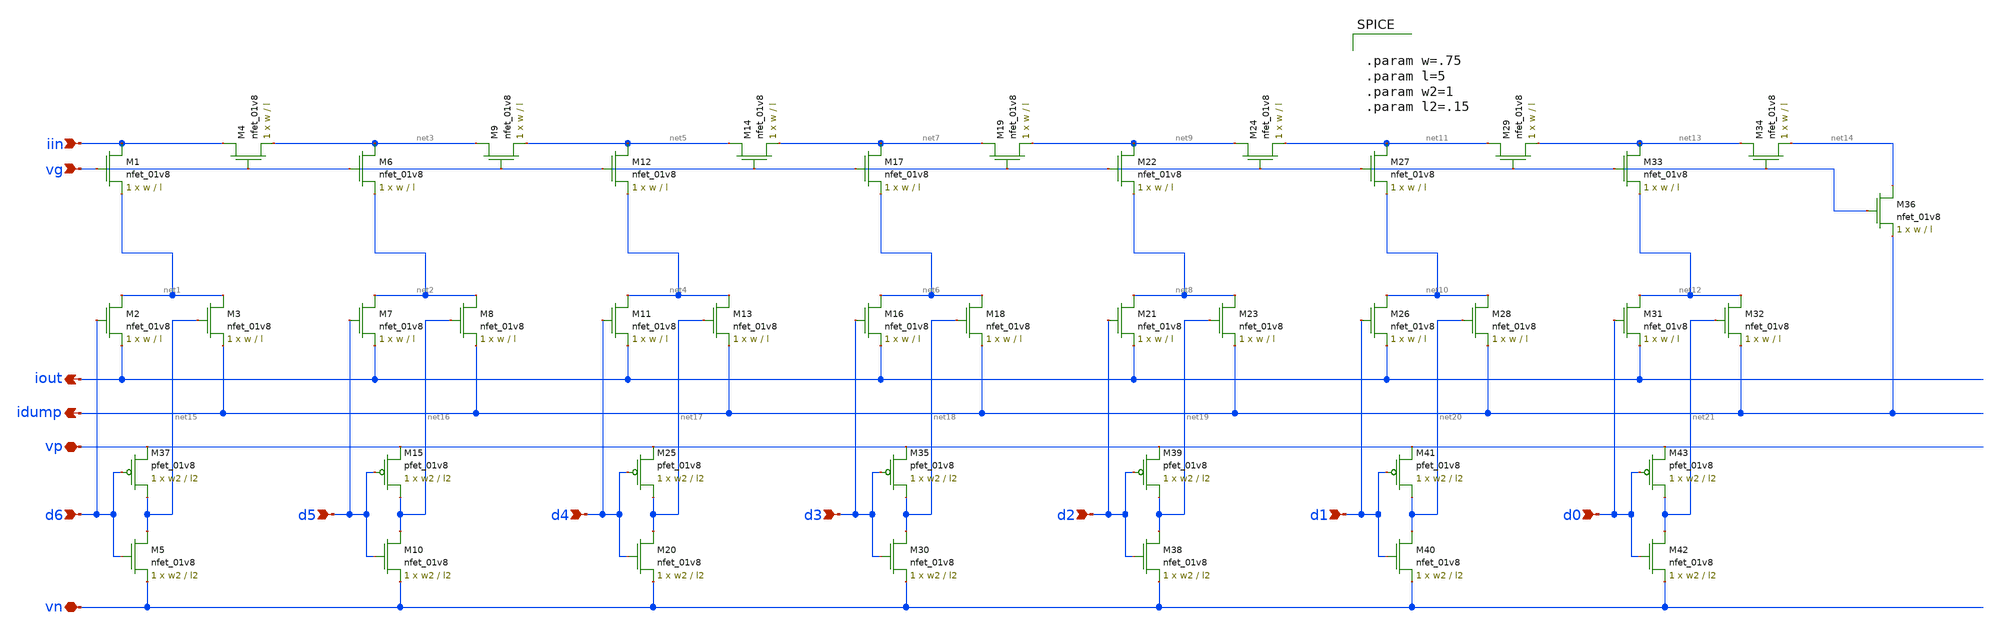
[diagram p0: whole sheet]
** sch_path: schematic/old/ladder.sch
**.subckt ladder iout idump iin vn vp d6 d5 d4 d3 d2 d1 d0 vg
*.opin iout
*.opin idump
*.ipin iin
*.iopin vn
*.iopin vp
*.ipin d6
*.ipin d5
*.ipin d4
*.ipin d3
*.ipin d2
*.ipin d1
*.ipin d0
*.ipin vg
XM1 iin vg net1 GND sky130_fd_pr__nfet_01v8 L=l W=w nf=1 ad='int((nf+1)/2) * W/nf * 0.29' as='int((nf+2)/2) * W/nf * 0.29'
+ pd='2*int((nf+1)/2) * (W/nf + 0.29)' ps='2*int((nf+2)/2) * (W/nf + 0.29)' nrd='0.29 / W' nrs='0.29 / W'
+ sa=0 sb=0 sd=0 mult=1 m=1
XM2 net1 d6 iout GND sky130_fd_pr__nfet_01v8 L=l W=w nf=1 ad='int((nf+1)/2) * W/nf * 0.29' as='int((nf+2)/2) * W/nf * 0.29'
+ pd='2*int((nf+1)/2) * (W/nf + 0.29)' ps='2*int((nf+2)/2) * (W/nf + 0.29)' nrd='0.29 / W' nrs='0.29 / W'
+ sa=0 sb=0 sd=0 mult=1 m=1
XM3 net1 net15 idump GND sky130_fd_pr__nfet_01v8 L=l W=w nf=1 ad='int((nf+1)/2) * W/nf * 0.29' as='int((nf+2)/2) * W/nf * 0.29'
+ pd='2*int((nf+1)/2) * (W/nf + 0.29)' ps='2*int((nf+2)/2) * (W/nf + 0.29)' nrd='0.29 / W' nrs='0.29 / W'
+ sa=0 sb=0 sd=0 mult=1 m=1
XM4 iin vg net3 GND sky130_fd_pr__nfet_01v8 L=l W=w nf=1 ad='int((nf+1)/2) * W/nf * 0.29' as='int((nf+2)/2) * W/nf * 0.29'
+ pd='2*int((nf+1)/2) * (W/nf + 0.29)' ps='2*int((nf+2)/2) * (W/nf + 0.29)' nrd='0.29 / W' nrs='0.29 / W'
+ sa=0 sb=0 sd=0 mult=1 m=1
XM5 net15 d6 vn GND sky130_fd_pr__nfet_01v8 L=l2 W=w2 nf=1 ad='int((nf+1)/2) * W/nf * 0.29' as='int((nf+2)/2) * W/nf * 0.29'
+ pd='2*int((nf+1)/2) * (W/nf + 0.29)' ps='2*int((nf+2)/2) * (W/nf + 0.29)' nrd='0.29 / W' nrs='0.29 / W'
+ sa=0 sb=0 sd=0 mult=1 m=1
XM6 net3 vg net2 GND sky130_fd_pr__nfet_01v8 L=l W=w nf=1 ad='int((nf+1)/2) * W/nf * 0.29' as='int((nf+2)/2) * W/nf * 0.29'
+ pd='2*int((nf+1)/2) * (W/nf + 0.29)' ps='2*int((nf+2)/2) * (W/nf + 0.29)' nrd='0.29 / W' nrs='0.29 / W'
+ sa=0 sb=0 sd=0 mult=1 m=1
XM7 net2 d5 iout GND sky130_fd_pr__nfet_01v8 L=l W=w nf=1 ad='int((nf+1)/2) * W/nf * 0.29' as='int((nf+2)/2) * W/nf * 0.29'
+ pd='2*int((nf+1)/2) * (W/nf + 0.29)' ps='2*int((nf+2)/2) * (W/nf + 0.29)' nrd='0.29 / W' nrs='0.29 / W'
+ sa=0 sb=0 sd=0 mult=1 m=1
XM8 net2 net16 idump GND sky130_fd_pr__nfet_01v8 L=l W=w nf=1 ad='int((nf+1)/2) * W/nf * 0.29' as='int((nf+2)/2) * W/nf * 0.29'
+ pd='2*int((nf+1)/2) * (W/nf + 0.29)' ps='2*int((nf+2)/2) * (W/nf + 0.29)' nrd='0.29 / W' nrs='0.29 / W'
+ sa=0 sb=0 sd=0 mult=1 m=1
XM9 net3 vg net5 GND sky130_fd_pr__nfet_01v8 L=l W=w nf=1 ad='int((nf+1)/2) * W/nf * 0.29' as='int((nf+2)/2) * W/nf * 0.29'
+ pd='2*int((nf+1)/2) * (W/nf + 0.29)' ps='2*int((nf+2)/2) * (W/nf + 0.29)' nrd='0.29 / W' nrs='0.29 / W'
+ sa=0 sb=0 sd=0 mult=1 m=1
XM11 net4 d4 iout GND sky130_fd_pr__nfet_01v8 L=l W=w nf=1 ad='int((nf+1)/2) * W/nf * 0.29' as='int((nf+2)/2) * W/nf * 0.29'
+ pd='2*int((nf+1)/2) * (W/nf + 0.29)' ps='2*int((nf+2)/2) * (W/nf + 0.29)' nrd='0.29 / W' nrs='0.29 / W'
+ sa=0 sb=0 sd=0 mult=1 m=1
XM12 net5 vg net4 GND sky130_fd_pr__nfet_01v8 L=l W=w nf=1 ad='int((nf+1)/2) * W/nf * 0.29' as='int((nf+2)/2) * W/nf * 0.29'
+ pd='2*int((nf+1)/2) * (W/nf + 0.29)' ps='2*int((nf+2)/2) * (W/nf + 0.29)' nrd='0.29 / W' nrs='0.29 / W'
+ sa=0 sb=0 sd=0 mult=1 m=1
XM13 net4 net17 idump GND sky130_fd_pr__nfet_01v8 L=l W=w nf=1 ad='int((nf+1)/2) * W/nf * 0.29' as='int((nf+2)/2) * W/nf * 0.29'
+ pd='2*int((nf+1)/2) * (W/nf + 0.29)' ps='2*int((nf+2)/2) * (W/nf + 0.29)' nrd='0.29 / W' nrs='0.29 / W'
+ sa=0 sb=0 sd=0 mult=1 m=1
XM14 net5 vg net7 GND sky130_fd_pr__nfet_01v8 L=l W=w nf=1 ad='int((nf+1)/2) * W/nf * 0.29' as='int((nf+2)/2) * W/nf * 0.29'
+ pd='2*int((nf+1)/2) * (W/nf + 0.29)' ps='2*int((nf+2)/2) * (W/nf + 0.29)' nrd='0.29 / W' nrs='0.29 / W'
+ sa=0 sb=0 sd=0 mult=1 m=1
XM16 net6 d3 iout GND sky130_fd_pr__nfet_01v8 L=l W=w nf=1 ad='int((nf+1)/2) * W/nf * 0.29' as='int((nf+2)/2) * W/nf * 0.29'
+ pd='2*int((nf+1)/2) * (W/nf + 0.29)' ps='2*int((nf+2)/2) * (W/nf + 0.29)' nrd='0.29 / W' nrs='0.29 / W'
+ sa=0 sb=0 sd=0 mult=1 m=1
XM17 net7 vg net6 GND sky130_fd_pr__nfet_01v8 L=l W=w nf=1 ad='int((nf+1)/2) * W/nf * 0.29' as='int((nf+2)/2) * W/nf * 0.29'
+ pd='2*int((nf+1)/2) * (W/nf + 0.29)' ps='2*int((nf+2)/2) * (W/nf + 0.29)' nrd='0.29 / W' nrs='0.29 / W'
+ sa=0 sb=0 sd=0 mult=1 m=1
XM18 net6 net18 idump GND sky130_fd_pr__nfet_01v8 L=l W=w nf=1 ad='int((nf+1)/2) * W/nf * 0.29' as='int((nf+2)/2) * W/nf * 0.29'
+ pd='2*int((nf+1)/2) * (W/nf + 0.29)' ps='2*int((nf+2)/2) * (W/nf + 0.29)' nrd='0.29 / W' nrs='0.29 / W'
+ sa=0 sb=0 sd=0 mult=1 m=1
XM19 net7 vg net9 GND sky130_fd_pr__nfet_01v8 L=l W=w nf=1 ad='int((nf+1)/2) * W/nf * 0.29' as='int((nf+2)/2) * W/nf * 0.29'
+ pd='2*int((nf+1)/2) * (W/nf + 0.29)' ps='2*int((nf+2)/2) * (W/nf + 0.29)' nrd='0.29 / W' nrs='0.29 / W'
+ sa=0 sb=0 sd=0 mult=1 m=1
XM21 net8 d2 iout GND sky130_fd_pr__nfet_01v8 L=l W=w nf=1 ad='int((nf+1)/2) * W/nf * 0.29' as='int((nf+2)/2) * W/nf * 0.29'
+ pd='2*int((nf+1)/2) * (W/nf + 0.29)' ps='2*int((nf+2)/2) * (W/nf + 0.29)' nrd='0.29 / W' nrs='0.29 / W'
+ sa=0 sb=0 sd=0 mult=1 m=1
XM22 net9 vg net8 GND sky130_fd_pr__nfet_01v8 L=l W=w nf=1 ad='int((nf+1)/2) * W/nf * 0.29' as='int((nf+2)/2) * W/nf * 0.29'
+ pd='2*int((nf+1)/2) * (W/nf + 0.29)' ps='2*int((nf+2)/2) * (W/nf + 0.29)' nrd='0.29 / W' nrs='0.29 / W'
+ sa=0 sb=0 sd=0 mult=1 m=1
XM23 net8 net19 idump GND sky130_fd_pr__nfet_01v8 L=l W=w nf=1 ad='int((nf+1)/2) * W/nf * 0.29' as='int((nf+2)/2) * W/nf * 0.29'
+ pd='2*int((nf+1)/2) * (W/nf + 0.29)' ps='2*int((nf+2)/2) * (W/nf + 0.29)' nrd='0.29 / W' nrs='0.29 / W'
+ sa=0 sb=0 sd=0 mult=1 m=1
XM24 net9 vg net11 GND sky130_fd_pr__nfet_01v8 L=l W=w nf=1 ad='int((nf+1)/2) * W/nf * 0.29' as='int((nf+2)/2) * W/nf * 0.29'
+ pd='2*int((nf+1)/2) * (W/nf + 0.29)' ps='2*int((nf+2)/2) * (W/nf + 0.29)' nrd='0.29 / W' nrs='0.29 / W'
+ sa=0 sb=0 sd=0 mult=1 m=1
XM26 net10 d1 iout GND sky130_fd_pr__nfet_01v8 L=l W=w nf=1 ad='int((nf+1)/2) * W/nf * 0.29' as='int((nf+2)/2) * W/nf * 0.29'
+ pd='2*int((nf+1)/2) * (W/nf + 0.29)' ps='2*int((nf+2)/2) * (W/nf + 0.29)' nrd='0.29 / W' nrs='0.29 / W'
+ sa=0 sb=0 sd=0 mult=1 m=1
XM27 net11 vg net10 GND sky130_fd_pr__nfet_01v8 L=l W=w nf=1 ad='int((nf+1)/2) * W/nf * 0.29' as='int((nf+2)/2) * W/nf * 0.29'
+ pd='2*int((nf+1)/2) * (W/nf + 0.29)' ps='2*int((nf+2)/2) * (W/nf + 0.29)' nrd='0.29 / W' nrs='0.29 / W'
+ sa=0 sb=0 sd=0 mult=1 m=1
XM28 net10 net20 idump GND sky130_fd_pr__nfet_01v8 L=l W=w nf=1 ad='int((nf+1)/2) * W/nf * 0.29' as='int((nf+2)/2) * W/nf * 0.29'
+ pd='2*int((nf+1)/2) * (W/nf + 0.29)' ps='2*int((nf+2)/2) * (W/nf + 0.29)' nrd='0.29 / W' nrs='0.29 / W'
+ sa=0 sb=0 sd=0 mult=1 m=1
XM29 net11 vg net13 GND sky130_fd_pr__nfet_01v8 L=l W=w nf=1 ad='int((nf+1)/2) * W/nf * 0.29' as='int((nf+2)/2) * W/nf * 0.29'
+ pd='2*int((nf+1)/2) * (W/nf + 0.29)' ps='2*int((nf+2)/2) * (W/nf + 0.29)' nrd='0.29 / W' nrs='0.29 / W'
+ sa=0 sb=0 sd=0 mult=1 m=1
XM31 net12 d0 iout GND sky130_fd_pr__nfet_01v8 L=l W=w nf=1 ad='int((nf+1)/2) * W/nf * 0.29' as='int((nf+2)/2) * W/nf * 0.29'
+ pd='2*int((nf+1)/2) * (W/nf + 0.29)' ps='2*int((nf+2)/2) * (W/nf + 0.29)' nrd='0.29 / W' nrs='0.29 / W'
+ sa=0 sb=0 sd=0 mult=1 m=1
XM32 net12 net21 idump GND sky130_fd_pr__nfet_01v8 L=l W=w nf=1 ad='int((nf+1)/2) * W/nf * 0.29' as='int((nf+2)/2) * W/nf * 0.29'
+ pd='2*int((nf+1)/2) * (W/nf + 0.29)' ps='2*int((nf+2)/2) * (W/nf + 0.29)' nrd='0.29 / W' nrs='0.29 / W'
+ sa=0 sb=0 sd=0 mult=1 m=1
XM33 net13 vg net12 GND sky130_fd_pr__nfet_01v8 L=l W=w nf=1 ad='int((nf+1)/2) * W/nf * 0.29' as='int((nf+2)/2) * W/nf * 0.29'
+ pd='2*int((nf+1)/2) * (W/nf + 0.29)' ps='2*int((nf+2)/2) * (W/nf + 0.29)' nrd='0.29 / W' nrs='0.29 / W'
+ sa=0 sb=0 sd=0 mult=1 m=1
XM34 net13 vg net14 GND sky130_fd_pr__nfet_01v8 L=l W=w nf=1 ad='int((nf+1)/2) * W/nf * 0.29' as='int((nf+2)/2) * W/nf * 0.29'
+ pd='2*int((nf+1)/2) * (W/nf + 0.29)' ps='2*int((nf+2)/2) * (W/nf + 0.29)' nrd='0.29 / W' nrs='0.29 / W'
+ sa=0 sb=0 sd=0 mult=1 m=1
XM36 net14 vg idump GND sky130_fd_pr__nfet_01v8 L=l W=w nf=1 ad='int((nf+1)/2) * W/nf * 0.29' as='int((nf+2)/2) * W/nf * 0.29'
+ pd='2*int((nf+1)/2) * (W/nf + 0.29)' ps='2*int((nf+2)/2) * (W/nf + 0.29)' nrd='0.29 / W' nrs='0.29 / W'
+ sa=0 sb=0 sd=0 mult=1 m=1
XM37 net15 d6 vp VDD sky130_fd_pr__pfet_01v8 L=l2 W=w2 nf=1 ad='int((nf+1)/2) * W/nf * 0.29' as='int((nf+2)/2) * W/nf * 0.29'
+ pd='2*int((nf+1)/2) * (W/nf + 0.29)' ps='2*int((nf+2)/2) * (W/nf + 0.29)' nrd='0.29 / W' nrs='0.29 / W'
+ sa=0 sb=0 sd=0 mult=1 m=1
XM10 net16 d5 vn GND sky130_fd_pr__nfet_01v8 L=l2 W=w2 nf=1 ad='int((nf+1)/2) * W/nf * 0.29' as='int((nf+2)/2) * W/nf * 0.29'
+ pd='2*int((nf+1)/2) * (W/nf + 0.29)' ps='2*int((nf+2)/2) * (W/nf + 0.29)' nrd='0.29 / W' nrs='0.29 / W'
+ sa=0 sb=0 sd=0 mult=1 m=1
XM15 net16 d5 vp VDD sky130_fd_pr__pfet_01v8 L=l2 W=w2 nf=1 ad='int((nf+1)/2) * W/nf * 0.29' as='int((nf+2)/2) * W/nf * 0.29'
+ pd='2*int((nf+1)/2) * (W/nf + 0.29)' ps='2*int((nf+2)/2) * (W/nf + 0.29)' nrd='0.29 / W' nrs='0.29 / W'
+ sa=0 sb=0 sd=0 mult=1 m=1
XM20 net17 d4 vn GND sky130_fd_pr__nfet_01v8 L=l2 W=w2 nf=1 ad='int((nf+1)/2) * W/nf * 0.29' as='int((nf+2)/2) * W/nf * 0.29'
+ pd='2*int((nf+1)/2) * (W/nf + 0.29)' ps='2*int((nf+2)/2) * (W/nf + 0.29)' nrd='0.29 / W' nrs='0.29 / W'
+ sa=0 sb=0 sd=0 mult=1 m=1
XM25 net17 d4 vp VDD sky130_fd_pr__pfet_01v8 L=l2 W=w2 nf=1 ad='int((nf+1)/2) * W/nf * 0.29' as='int((nf+2)/2) * W/nf * 0.29'
+ pd='2*int((nf+1)/2) * (W/nf + 0.29)' ps='2*int((nf+2)/2) * (W/nf + 0.29)' nrd='0.29 / W' nrs='0.29 / W'
+ sa=0 sb=0 sd=0 mult=1 m=1
XM30 net18 d3 vn GND sky130_fd_pr__nfet_01v8 L=l2 W=w2 nf=1 ad='int((nf+1)/2) * W/nf * 0.29' as='int((nf+2)/2) * W/nf * 0.29'
+ pd='2*int((nf+1)/2) * (W/nf + 0.29)' ps='2*int((nf+2)/2) * (W/nf + 0.29)' nrd='0.29 / W' nrs='0.29 / W'
+ sa=0 sb=0 sd=0 mult=1 m=1
XM35 net18 d3 vp VDD sky130_fd_pr__pfet_01v8 L=l2 W=w2 nf=1 ad='int((nf+1)/2) * W/nf * 0.29' as='int((nf+2)/2) * W/nf * 0.29'
+ pd='2*int((nf+1)/2) * (W/nf + 0.29)' ps='2*int((nf+2)/2) * (W/nf + 0.29)' nrd='0.29 / W' nrs='0.29 / W'
+ sa=0 sb=0 sd=0 mult=1 m=1
XM38 net19 d2 vn GND sky130_fd_pr__nfet_01v8 L=l2 W=w2 nf=1 ad='int((nf+1)/2) * W/nf * 0.29' as='int((nf+2)/2) * W/nf * 0.29'
+ pd='2*int((nf+1)/2) * (W/nf + 0.29)' ps='2*int((nf+2)/2) * (W/nf + 0.29)' nrd='0.29 / W' nrs='0.29 / W'
+ sa=0 sb=0 sd=0 mult=1 m=1
XM39 net19 d2 vp VDD sky130_fd_pr__pfet_01v8 L=l2 W=w2 nf=1 ad='int((nf+1)/2) * W/nf * 0.29' as='int((nf+2)/2) * W/nf * 0.29'
+ pd='2*int((nf+1)/2) * (W/nf + 0.29)' ps='2*int((nf+2)/2) * (W/nf + 0.29)' nrd='0.29 / W' nrs='0.29 / W'
+ sa=0 sb=0 sd=0 mult=1 m=1
XM40 net20 d1 vn GND sky130_fd_pr__nfet_01v8 L=l2 W=w2 nf=1 ad='int((nf+1)/2) * W/nf * 0.29' as='int((nf+2)/2) * W/nf * 0.29'
+ pd='2*int((nf+1)/2) * (W/nf + 0.29)' ps='2*int((nf+2)/2) * (W/nf + 0.29)' nrd='0.29 / W' nrs='0.29 / W'
+ sa=0 sb=0 sd=0 mult=1 m=1
XM41 net20 d1 vp VDD sky130_fd_pr__pfet_01v8 L=l2 W=w2 nf=1 ad='int((nf+1)/2) * W/nf * 0.29' as='int((nf+2)/2) * W/nf * 0.29'
+ pd='2*int((nf+1)/2) * (W/nf + 0.29)' ps='2*int((nf+2)/2) * (W/nf + 0.29)' nrd='0.29 / W' nrs='0.29 / W'
+ sa=0 sb=0 sd=0 mult=1 m=1
XM42 net21 d0 vn GND sky130_fd_pr__nfet_01v8 L=l2 W=w2 nf=1 ad='int((nf+1)/2) * W/nf * 0.29' as='int((nf+2)/2) * W/nf * 0.29'
+ pd='2*int((nf+1)/2) * (W/nf + 0.29)' ps='2*int((nf+2)/2) * (W/nf + 0.29)' nrd='0.29 / W' nrs='0.29 / W'
+ sa=0 sb=0 sd=0 mult=1 m=1
XM43 net21 d0 vp VDD sky130_fd_pr__pfet_01v8 L=l2 W=w2 nf=1 ad='int((nf+1)/2) * W/nf * 0.29' as='int((nf+2)/2) * W/nf * 0.29'
+ pd='2*int((nf+1)/2) * (W/nf + 0.29)' ps='2*int((nf+2)/2) * (W/nf + 0.29)' nrd='0.29 / W' nrs='0.29 / W'
+ sa=0 sb=0 sd=0 mult=1 m=1
**** begin user architecture code


.param w=.75
.param l=5
.param w2=1
.param l2=.15


**** end user architecture code
**.ends
.end
